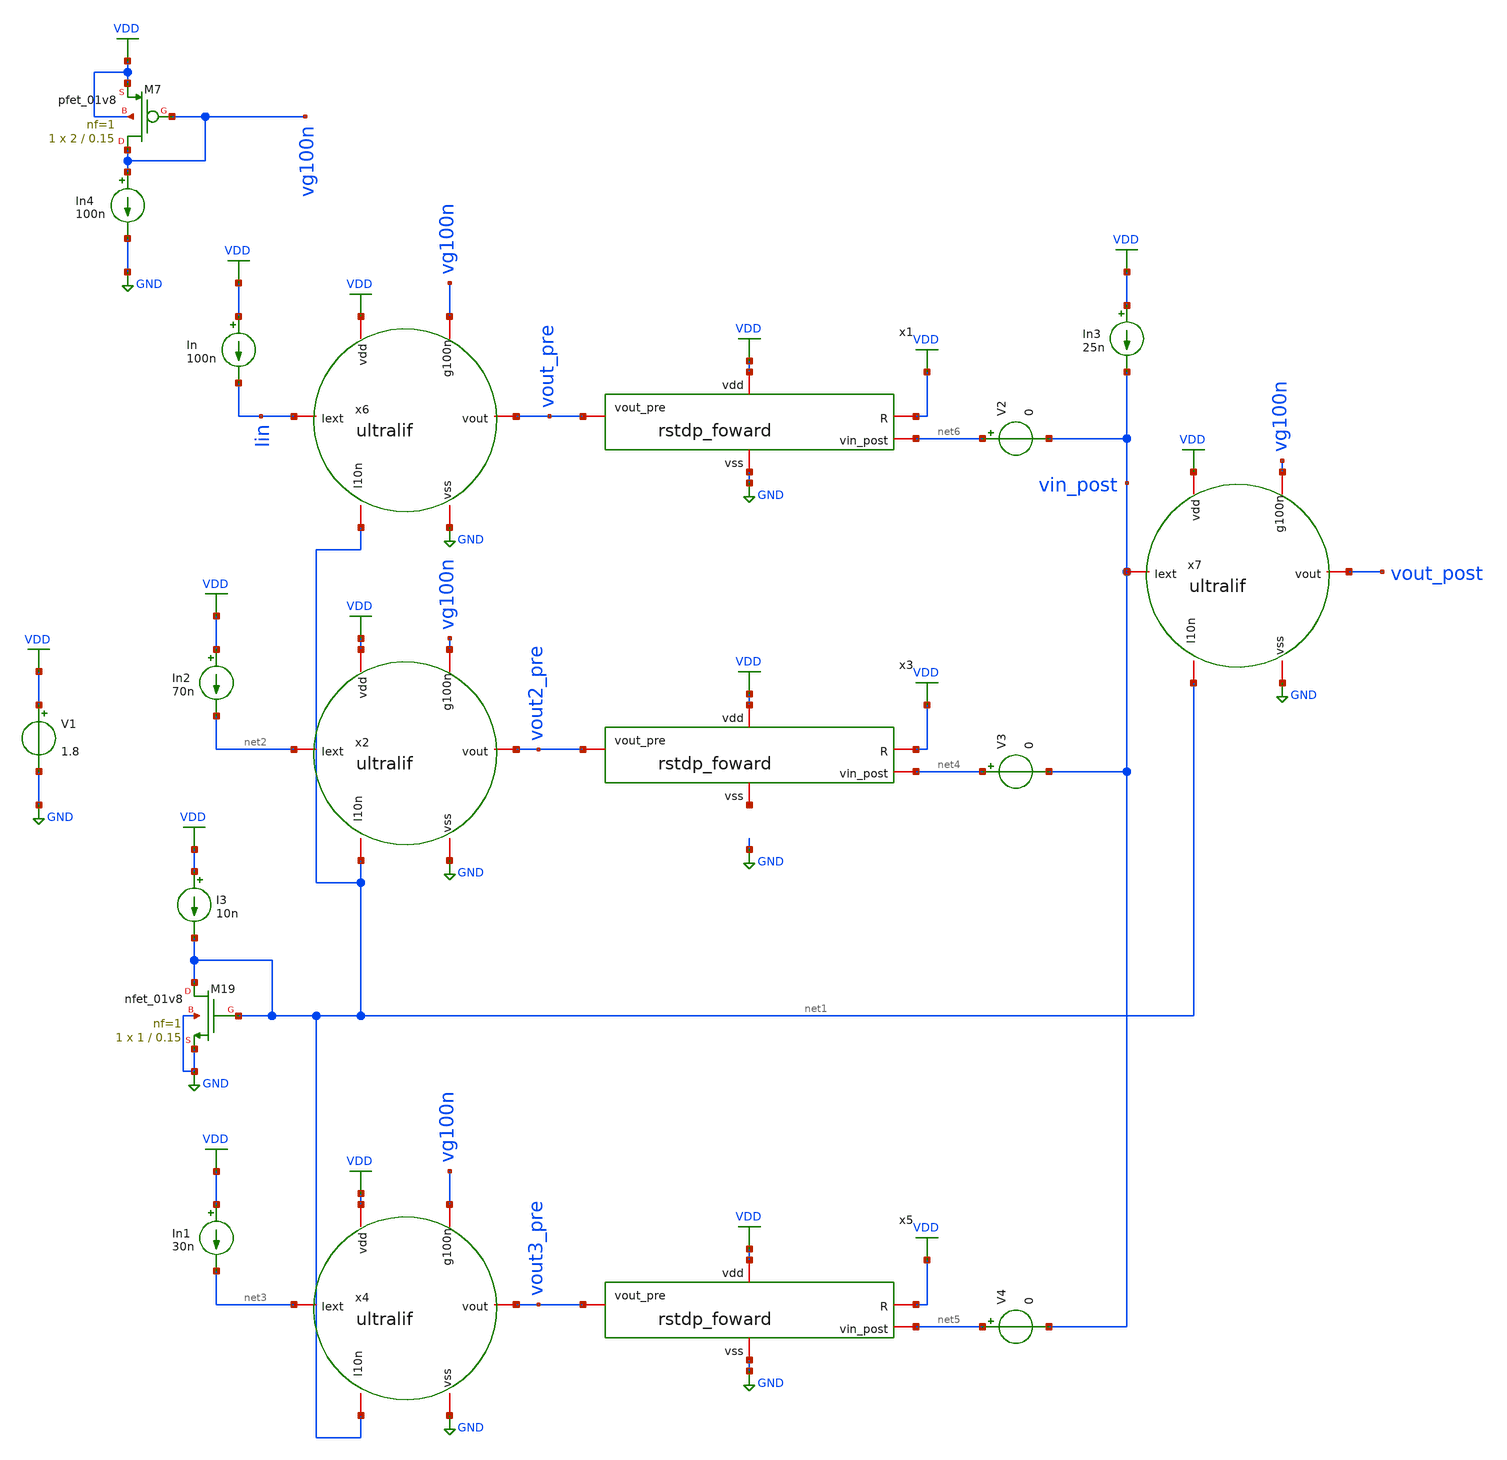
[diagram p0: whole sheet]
** sch_path: tb_3_1_foward.sch
**.subckt tb_3_1_foward
V1 VDD GND 1.8
x6 VDD Iin vout_pre net1 GND vg100n ultralif
x7 VDD vin_post vout_post net1 GND vg100n ultralif
XM19 net1 net1 GND GND sky130_fd_pr__nfet_01v8 L=0.15 W=1 nf=1 ad='int((nf+1)/2) * W/nf * 0.29' as='int((nf+2)/2) * W/nf * 0.29'
+ pd='2*int((nf+1)/2) * (W/nf + 0.29)' ps='2*int((nf+2)/2) * (W/nf + 0.29)' nrd='0.29 / W' nrs='0.29 / W'
+ sa=0 sb=0 sd=0 mult=1 m=1
I3 VDD net1 10n
In VDD Iin 100n
x2 VDD net2 vout2_pre net1 GND vg100n ultralif
In2 VDD net2 70n
x4 VDD net3 vout3_pre net1 GND vg100n ultralif
In1 VDD net3 30n
In3 VDD vin_post 25n
XM7 vg100n vg100n VDD VDD sky130_fd_pr__pfet_01v8 L=0.15 W=2 nf=1 ad='int((nf+1)/2) * W/nf * 0.29' as='int((nf+2)/2) * W/nf * 0.29'
+ pd='2*int((nf+1)/2) * (W/nf + 0.29)' ps='2*int((nf+2)/2) * (W/nf + 0.29)' nrd='0.29 / W' nrs='0.29 / W'
+ sa=0 sb=0 sd=0 mult=1 m=1
In4 vg100n GND 100n
V2 net6 vin_post 0
V3 net4 vin_post 0
V4 net5 vin_post 0
x1 VDD VDD GND vout_pre net6 rstdp_foward
x3 VDD VDD net7 vout2_pre net4 rstdp_foward
x5 VDD VDD GND vout3_pre net5 rstdp_foward
**** begin user architecture code
.lib $::SKYWATER_MODELS/sky130.lib.spice tt

** opencircuitdesign pdks install
.inc $::SKYWATER_MODELS/rram_v0.spice

**** end user architecture code
**.ends

* expanding   symbol:  /home/alex/Desktop/EDA/SNN_IPN/Neuron/ultralif/ultralif.sym # of pins=6
** sym_path: Neuron/ultralif/ultralif.sym
** sch_path: Neuron/ultralif/ultralif.sch
.subckt ultralif vdd Iext vout I10n vss g100n
*.iopin Iext
*.iopin vout
*.iopin vss
*.iopin I10n
*.iopin vdd
*.iopin g100n
XM1 net2 net2 vm vdd sky130_fd_pr__pfet_01v8 L=10 W=1 nf=1 ad='int((nf+1)/2) * W/nf * 0.29' as='int((nf+2)/2) * W/nf * 0.29'
+ pd='2*int((nf+1)/2) * (W/nf + 0.29)' ps='2*int((nf+2)/2) * (W/nf + 0.29)' nrd='0.29 / W' nrs='0.29 / W'
+ sa=0 sb=0 sd=0 mult=1 m=1
XM2 net2 net1 vm vdd sky130_fd_pr__pfet_01v8 L=0.15 W=1.5 nf=1 ad='int((nf+1)/2) * W/nf * 0.29' as='int((nf+2)/2) * W/nf * 0.29'
+ pd='2*int((nf+1)/2) * (W/nf + 0.29)' ps='2*int((nf+2)/2) * (W/nf + 0.29)' nrd='0.29 / W' nrs='0.29 / W'
+ sa=0 sb=0 sd=0 mult=1 m=1
XM3 net1 net1 vm vdd sky130_fd_pr__pfet_01v8 L=0.15 W=5 nf=1 ad='int((nf+1)/2) * W/nf * 0.29' as='int((nf+2)/2) * W/nf * 0.29'
+ pd='2*int((nf+1)/2) * (W/nf + 0.29)' ps='2*int((nf+2)/2) * (W/nf + 0.29)' nrd='0.29 / W' nrs='0.29 / W'
+ sa=0 sb=0 sd=0 mult=2 m=2
XM4 net1 net2 vss vss sky130_fd_pr__nfet_01v8 L=4 W=1 nf=1 ad='int((1 + 1)/2) * 1 / 1 * 0.29' as='int((1 + 2)/2) * 1 / 1 * 0.29'
+ pd='2*int((1 + 1)/2) * (1 / 1 + 0.29)' ps='2*int((1 + 2)/2) * (1 / 1 + 0.29)' nrd='0.29 / 1 ' nrs='0.29 / 1 '
+ sa=0 sb=0 sd=0 mult=1 m=1
C1 vm vss 0.1p m=1
XM9 vm net2 Iext vdd sky130_fd_pr__pfet_01v8 L=0.15 W=2 nf=1 ad='int((nf+1)/2) * W/nf * 0.29' as='int((nf+2)/2) * W/nf * 0.29'
+ pd='2*int((nf+1)/2) * (W/nf + 0.29)' ps='2*int((nf+2)/2) * (W/nf + 0.29)' nrd='0.29 / W' nrs='0.29 / W'
+ sa=0 sb=0 sd=0 mult=1 m=1
XM10 net2 I10n vss vss sky130_fd_pr__nfet_01v8 L=0.15 W=1 nf=1 ad='int((1 + 1)/2) * 1 / 1 * 0.29' as='int((1 + 2)/2) * 1 / 1 * 0.29'
+ pd='2*int((1 + 1)/2) * (1 / 1 + 0.29)' ps='2*int((1 + 2)/2) * (1 / 1 + 0.29)' nrd='0.29 / 1 ' nrs='0.29 / 1 '
+ sa=0 sb=0 sd=0 mult=1 m=1
XM5 vout net2 vss vss sky130_fd_pr__nfet_01v8 L=0.15 W=1 nf=1 ad='int((1 + 1)/2) * 1 / 1 * 0.29' as='int((1 + 2)/2) * 1 / 1 * 0.29'
+ pd='2*int((1 + 1)/2) * (1 / 1 + 0.29)' ps='2*int((1 + 2)/2) * (1 / 1 + 0.29)' nrd='0.29 / 1 ' nrs='0.29 / 1 '
+ sa=0 sb=0 sd=0 mult=1 m=1
XM6 vout g100n vdd vdd sky130_fd_pr__pfet_01v8 L=0.15 W=2 nf=1 ad='int((nf+1)/2) * W/nf * 0.29' as='int((nf+2)/2) * W/nf * 0.29'
+ pd='2*int((nf+1)/2) * (W/nf + 0.29)' ps='2*int((nf+2)/2) * (W/nf + 0.29)' nrd='0.29 / W' nrs='0.29 / W'
+ sa=0 sb=0 sd=0 mult=1 m=1
.ends


* expanding   symbol:  /home/alex/Desktop/EDA/SNN_IPN/Synapse/rstdp_foward.sym # of pins=5
** sym_path: Synapse/rstdp_foward.sym
** sch_path: Synapse/rstdp_foward.sch
.subckt rstdp_foward vdd R vss vout_pre vin_post
*.iopin vdd
*.iopin vss
*.iopin R
*.iopin vin_post
*.iopin vout_pre
XR2 te be rram_v0
XM2 vpre R be vss sky130_fd_pr__nfet_01v8 L=0.15 W=7.5 nf=1 ad='int((nf+1)/2) * W/nf * 0.29' as='int((nf+2)/2) * W/nf * 0.29'
+ pd='2*int((nf+1)/2) * (W/nf + 0.29)' ps='2*int((nf+2)/2) * (W/nf + 0.29)' nrd='0.29 / W' nrs='0.29 / W'
+ sa=0 sb=0 sd=0 mult=1 m=1
XM3 te R net1 vss sky130_fd_pr__nfet_01v8 L=0.15 W=7.5 nf=1 ad='int((nf+1)/2) * W/nf * 0.29' as='int((nf+2)/2) * W/nf * 0.29'
+ pd='2*int((nf+1)/2) * (W/nf + 0.29)' ps='2*int((nf+2)/2) * (W/nf + 0.29)' nrd='0.29 / W' nrs='0.29 / W'
+ sa=0 sb=0 sd=0 mult=1 m=1
XM1 te R vpre vdd sky130_fd_pr__pfet_01v8 L=0.15 W=15 nf=1 ad='int((nf+1)/2) * W/nf * 0.29' as='int((nf+2)/2) * W/nf * 0.29'
+ pd='2*int((nf+1)/2) * (W/nf + 0.29)' ps='2*int((nf+2)/2) * (W/nf + 0.29)' nrd='0.29 / W' nrs='0.29 / W'
+ sa=0 sb=0 sd=0 mult=2 m=2
XM4 net1 R be vdd sky130_fd_pr__pfet_01v8 L=0.15 W=15 nf=1 ad='int((nf+1)/2) * W/nf * 0.29' as='int((nf+2)/2) * W/nf * 0.29'
+ pd='2*int((nf+1)/2) * (W/nf + 0.29)' ps='2*int((nf+2)/2) * (W/nf + 0.29)' nrd='0.29 / W' nrs='0.29 / W'
+ sa=0 sb=0 sd=0 mult=2 m=2
XM6 vpre vout_pre vss vss sky130_fd_pr__nfet_01v8 L=0.15 W=1 nf=1 ad='int((1 + 1)/2) * 1 / 1 * 0.29'
+ as='int((1 + 2)/2) * 1 / 1 * 0.29' pd='2*int((1 + 1)/2) * (1 / 1 + 0.29)' ps='2*int((1 + 2)/2) * (1 / 1 + 0.29)'
+ nrd='0.29 / 1 ' nrs='0.29 / 1 ' sa=0 sb=0 sd=0 mult=1 m=1
XM8 vpre vout_pre vdd vdd sky130_fd_pr__pfet_01v8 L=0.15 W=2 nf=1 ad='int((nf+1)/2) * W/nf * 0.29' as='int((nf+2)/2) * W/nf * 0.29'
+ pd='2*int((nf+1)/2) * (W/nf + 0.29)' ps='2*int((nf+2)/2) * (W/nf + 0.29)' nrd='0.29 / W' nrs='0.29 / W'
+ sa=0 sb=0 sd=0 mult=1 m=1
XM5 net1 net1 vin_post vss sky130_fd_pr__nfet_01v8 L=0.15 W=1 nf=1 ad='int((1 + 1)/2) * 1 / 1 * 0.29'
+ as='int((1 + 2)/2) * 1 / 1 * 0.29' pd='2*int((1 + 1)/2) * (1 / 1 + 0.29)' ps='2*int((1 + 2)/2) * (1 / 1 + 0.29)'
+ nrd='0.29 / 1 ' nrs='0.29 / 1 ' sa=0 sb=0 sd=0 mult=1 m=1
.ends

.GLOBAL VDD
.GLOBAL GND
**** begin user architecture code


*.options savecurrents
.tran 50n 200u uic
.control
	run
	write tb_3_1_mirror.raw
.endc


**** end user architecture code
.end
